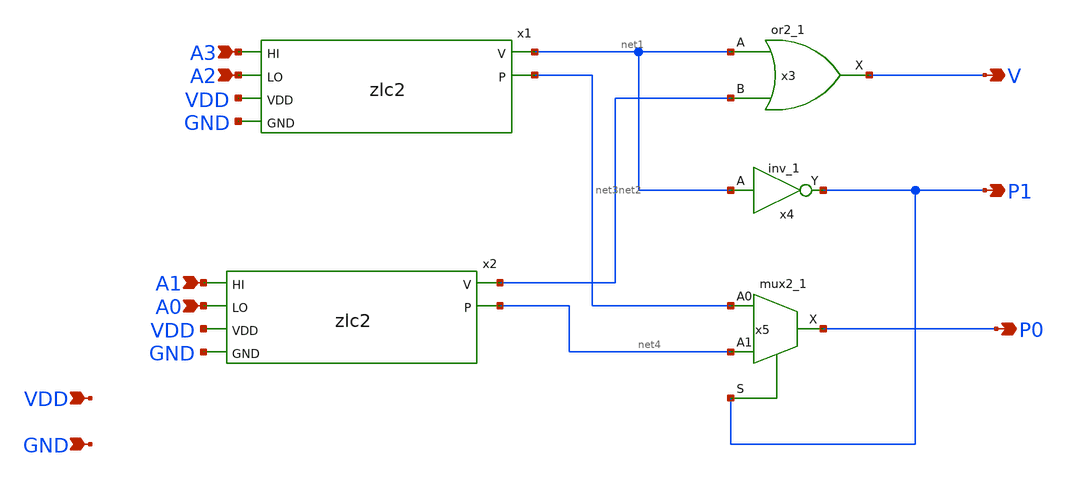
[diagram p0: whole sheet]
** sch_path: xschem/zlc4.sch
**.subckt zlc4 A3 A2 A1 A0 V P1 P0 VDD GND
*.ipin A3
*.ipin A2
*.ipin A1
*.ipin A0
*.opin V
*.opin P1
*.opin P0
*.ipin VDD
*.ipin GND
x3 net1 net2 GND GND VDD VDD V sky130_fd_sc_hd__or2_1
x4 net1 GND GND VDD VDD P1 sky130_fd_sc_hd__inv_1
x5 net3 net4 P1 GND GND VDD VDD P0 sky130_fd_sc_hd__mux2_1
x1 A3 net1 A2 net3 VDD GND zlc2
x2 A1 net2 A0 net4 VDD GND zlc2
**.ends

* expanding   symbol:  zlc2.sym # of pins=6
** sym_path: xschem/zlc2.sym
** sch_path: xschem/zlc2.sch
.subckt zlc2 HI V LO P VDD GND
*.ipin HI
*.ipin LO
*.opin V
*.opin P
*.ipin VDD
*.ipin GND
x1 HI LO GND GND VDD VDD V sky130_fd_sc_hd__or2_1
x2 HI GND GND VDD VDD P sky130_fd_sc_hd__inv_1
.ends

.end
